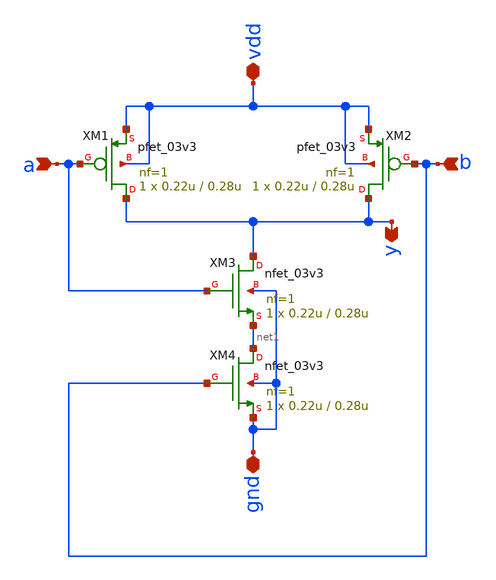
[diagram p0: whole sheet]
** sch_path: nand.sch
**.subckt nand gnd vdd a b y
*.iopin gnd
*.iopin vdd
*.ipin a
*.ipin b
*.opin y
XM1 y a vdd vdd pfet_03v3 L=0.28u W=0.22u nf=1 ad='int((nf+1)/2) * W/nf * 0.18u' as='int((nf+2)/2) * W/nf * 0.18u'
+ pd='2*int((nf+1)/2) * (W/nf + 0.18u)' ps='2*int((nf+2)/2) * (W/nf + 0.18u)' nrd='0.18u / W' nrs='0.18u / W'
+ sa=0 sb=0 sd=0 m=1
XM2 y b vdd vdd pfet_03v3 L=0.28u W=0.22u nf=1 ad='int((nf+1)/2) * W/nf * 0.18u' as='int((nf+2)/2) * W/nf * 0.18u'
+ pd='2*int((nf+1)/2) * (W/nf + 0.18u)' ps='2*int((nf+2)/2) * (W/nf + 0.18u)' nrd='0.18u / W' nrs='0.18u / W'
+ sa=0 sb=0 sd=0 m=1
XM3 y a net1 gnd nfet_03v3 L=0.28u W=0.22u nf=1 ad='int((nf+1)/2) * W/nf * 0.18u' as='int((nf+2)/2) * W/nf * 0.18u'
+ pd='2*int((nf+1)/2) * (W/nf + 0.18u)' ps='2*int((nf+2)/2) * (W/nf + 0.18u)' nrd='0.18u / W' nrs='0.18u / W'
+ sa=0 sb=0 sd=0 m=1
XM4 net1 b gnd gnd nfet_03v3 L=0.28u W=0.22u nf=1 ad='int((nf+1)/2) * W/nf * 0.18u' as='int((nf+2)/2) * W/nf * 0.18u'
+ pd='2*int((nf+1)/2) * (W/nf + 0.18u)' ps='2*int((nf+2)/2) * (W/nf + 0.18u)' nrd='0.18u / W' nrs='0.18u / W'
+ sa=0 sb=0 sd=0 m=1
**.ends
.end
